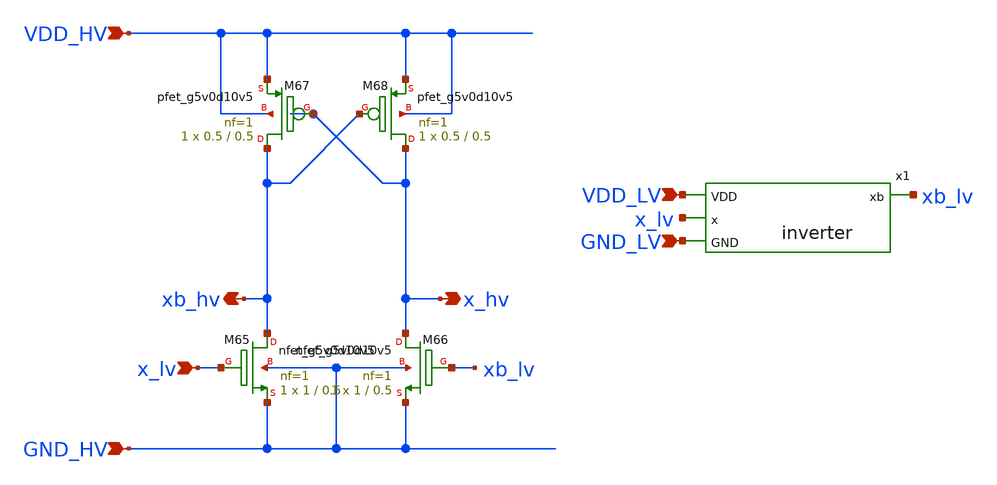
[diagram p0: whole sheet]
** sch_path: xschem/level_shifter_up.sch
**.subckt level_shifter_up VDD_HV GND_HV x_lv VDD_LV x_hv xb_hv GND_LV
*.ipin VDD_HV
*.ipin GND_HV
*.ipin x_lv
*.ipin VDD_LV
*.opin x_hv
*.opin xb_hv
*.ipin GND_LV
XM65 xb_hv x_lv GND_HV GND_HV sky130_fd_pr__nfet_g5v0d10v5 L=0.5 W=1 nf=1 ad='int((nf+1)/2) * W/nf * 0.29'
+ as='int((nf+2)/2) * W/nf * 0.29' pd='2*int((nf+1)/2) * (W/nf + 0.29)' ps='2*int((nf+2)/2) * (W/nf + 0.29)'
+ nrd='0.29 / W' nrs='0.29 / W' sa=0 sb=0 sd=0 mult=1 m=1
XM66 x_hv xb_lv GND_HV GND_HV sky130_fd_pr__nfet_g5v0d10v5 L=0.5 W=1 nf=1 ad='int((nf+1)/2) * W/nf * 0.29'
+ as='int((nf+2)/2) * W/nf * 0.29' pd='2*int((nf+1)/2) * (W/nf + 0.29)' ps='2*int((nf+2)/2) * (W/nf + 0.29)'
+ nrd='0.29 / W' nrs='0.29 / W' sa=0 sb=0 sd=0 mult=1 m=1
XM67 xb_hv x_hv VDD_HV VDD_HV sky130_fd_pr__pfet_g5v0d10v5 L=0.5 W=0.5 nf=1 ad='int((nf+1)/2) * W/nf * 0.29'
+ as='int((nf+2)/2) * W/nf * 0.29' pd='2*int((nf+1)/2) * (W/nf + 0.29)' ps='2*int((nf+2)/2) * (W/nf + 0.29)'
+ nrd='0.29 / W' nrs='0.29 / W' sa=0 sb=0 sd=0 mult=1 m=1
XM68 x_hv xb_hv VDD_HV VDD_HV sky130_fd_pr__pfet_g5v0d10v5 L=0.5 W=0.5 nf=1 ad='int((nf+1)/2) * W/nf * 0.29'
+ as='int((nf+2)/2) * W/nf * 0.29' pd='2*int((nf+1)/2) * (W/nf + 0.29)' ps='2*int((nf+2)/2) * (W/nf + 0.29)'
+ nrd='0.29 / W' nrs='0.29 / W' sa=0 sb=0 sd=0 mult=1 m=1
x1 VDD_LV xb_lv x_lv GND_LV inverter
**.ends

* expanding   symbol:  sky130_ak_ip__comparator/xschem/inverter.sym # of pins=4
** sym_path: xschem/inverter.sym
** sch_path: xschem/inverter.sch
.subckt inverter VDD xb x GND
*.ipin VDD
*.ipin GND
*.opin xb
*.ipin x
XM31 xb x VDD VDD sky130_fd_pr__pfet_01v8 L=1 W=2 nf=1 ad='int((nf+1)/2) * W/nf * 0.29' as='int((nf+2)/2) * W/nf * 0.29'
+ pd='2*int((nf+1)/2) * (W/nf + 0.29)' ps='2*int((nf+2)/2) * (W/nf + 0.29)' nrd='0.29 / W' nrs='0.29 / W'
+ sa=0 sb=0 sd=0 mult=1 m=1
XM44 xb x GND GND sky130_fd_pr__nfet_01v8 L=1 W=1 nf=1 ad='int((nf+1)/2) * W/nf * 0.29' as='int((nf+2)/2) * W/nf * 0.29'
+ pd='2*int((nf+1)/2) * (W/nf + 0.29)' ps='2*int((nf+2)/2) * (W/nf + 0.29)' nrd='0.29 / W' nrs='0.29 / W'
+ sa=0 sb=0 sd=0 mult=1 m=1
.ends

.end
